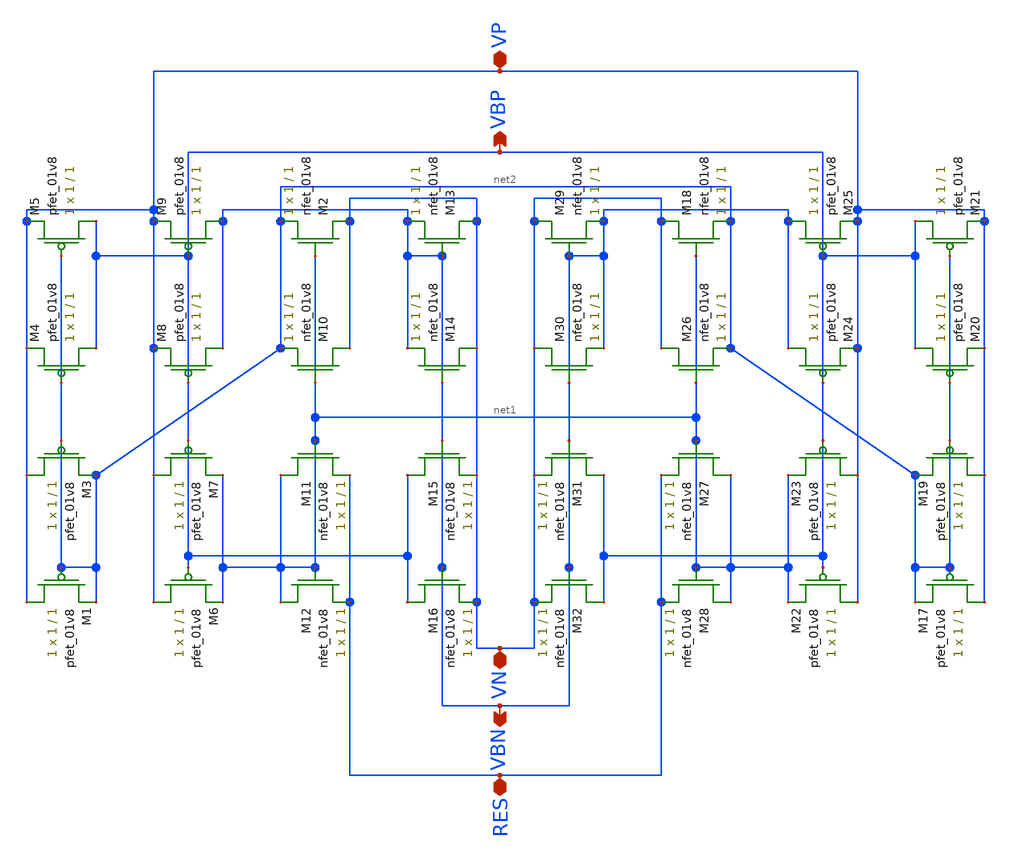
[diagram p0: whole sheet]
** sch_path: LDS/LDS_bbg.sch
**.subckt LDS_bbg VN VBN RES VP VBP
*.iopin VN
*.opin VBN
*.iopin RES
*.iopin VP
*.opin VBP
XM1 VP net2 net2 VDD sky130_fd_pr__pfet_01v8 L=1 W=1 nf=1 ad='int((nf+1)/2) * W/nf * 0.29' as='int((nf+2)/2) * W/nf * 0.29'
+ pd='2*int((nf+1)/2) * (W/nf + 0.29)' ps='2*int((nf+2)/2) * (W/nf + 0.29)' nrd='0.29 / W' nrs='0.29 / W'
+ sa=0 sb=0 sd=0 mult=1 m=1
XM2 VN net1 net2 GND sky130_fd_pr__nfet_01v8 L=1 W=1 nf=1 ad='int((nf+1)/2) * W/nf * 0.29' as='int((nf+2)/2) * W/nf * 0.29'
+ pd='2*int((nf+1)/2) * (W/nf + 0.29)' ps='2*int((nf+2)/2) * (W/nf + 0.29)' nrd='0.29 / W' nrs='0.29 / W'
+ sa=0 sb=0 sd=0 mult=1 m=1
XM3 VP net2 net2 VDD sky130_fd_pr__pfet_01v8 L=1 W=1 nf=1 ad='int((nf+1)/2) * W/nf * 0.29' as='int((nf+2)/2) * W/nf * 0.29'
+ pd='2*int((nf+1)/2) * (W/nf + 0.29)' ps='2*int((nf+2)/2) * (W/nf + 0.29)' nrd='0.29 / W' nrs='0.29 / W'
+ sa=0 sb=0 sd=0 mult=1 m=1
XM4 VBP net2 VP VDD sky130_fd_pr__pfet_01v8 L=1 W=1 nf=1 ad='int((nf+1)/2) * W/nf * 0.29' as='int((nf+2)/2) * W/nf * 0.29'
+ pd='2*int((nf+1)/2) * (W/nf + 0.29)' ps='2*int((nf+2)/2) * (W/nf + 0.29)' nrd='0.29 / W' nrs='0.29 / W'
+ sa=0 sb=0 sd=0 mult=1 m=1
XM5 VBP net2 VP VDD sky130_fd_pr__pfet_01v8 L=1 W=1 nf=1 ad='int((nf+1)/2) * W/nf * 0.29' as='int((nf+2)/2) * W/nf * 0.29'
+ pd='2*int((nf+1)/2) * (W/nf + 0.29)' ps='2*int((nf+2)/2) * (W/nf + 0.29)' nrd='0.29 / W' nrs='0.29 / W'
+ sa=0 sb=0 sd=0 mult=1 m=1
XM6 VP VBP net1 VDD sky130_fd_pr__pfet_01v8 L=1 W=1 nf=1 ad='int((nf+1)/2) * W/nf * 0.29' as='int((nf+2)/2) * W/nf * 0.29'
+ pd='2*int((nf+1)/2) * (W/nf + 0.29)' ps='2*int((nf+2)/2) * (W/nf + 0.29)' nrd='0.29 / W' nrs='0.29 / W'
+ sa=0 sb=0 sd=0 mult=1 m=1
XM7 VP VBP net1 VDD sky130_fd_pr__pfet_01v8 L=1 W=1 nf=1 ad='int((nf+1)/2) * W/nf * 0.29' as='int((nf+2)/2) * W/nf * 0.29'
+ pd='2*int((nf+1)/2) * (W/nf + 0.29)' ps='2*int((nf+2)/2) * (W/nf + 0.29)' nrd='0.29 / W' nrs='0.29 / W'
+ sa=0 sb=0 sd=0 mult=1 m=1
XM8 VBN VBP VP VDD sky130_fd_pr__pfet_01v8 L=1 W=1 nf=1 ad='int((nf+1)/2) * W/nf * 0.29' as='int((nf+2)/2) * W/nf * 0.29'
+ pd='2*int((nf+1)/2) * (W/nf + 0.29)' ps='2*int((nf+2)/2) * (W/nf + 0.29)' nrd='0.29 / W' nrs='0.29 / W'
+ sa=0 sb=0 sd=0 mult=1 m=1
XM9 VBN VBP VP VDD sky130_fd_pr__pfet_01v8 L=1 W=1 nf=1 ad='int((nf+1)/2) * W/nf * 0.29' as='int((nf+2)/2) * W/nf * 0.29'
+ pd='2*int((nf+1)/2) * (W/nf + 0.29)' ps='2*int((nf+2)/2) * (W/nf + 0.29)' nrd='0.29 / W' nrs='0.29 / W'
+ sa=0 sb=0 sd=0 mult=1 m=1
XM10 VN net1 net2 GND sky130_fd_pr__nfet_01v8 L=1 W=1 nf=1 ad='int((nf+1)/2) * W/nf * 0.29' as='int((nf+2)/2) * W/nf * 0.29'
+ pd='2*int((nf+1)/2) * (W/nf + 0.29)' ps='2*int((nf+2)/2) * (W/nf + 0.29)' nrd='0.29 / W' nrs='0.29 / W'
+ sa=0 sb=0 sd=0 mult=1 m=1
XM11 net1 net1 RES GND sky130_fd_pr__nfet_01v8 L=1 W=1 nf=1 ad='int((nf+1)/2) * W/nf * 0.29' as='int((nf+2)/2) * W/nf * 0.29'
+ pd='2*int((nf+1)/2) * (W/nf + 0.29)' ps='2*int((nf+2)/2) * (W/nf + 0.29)' nrd='0.29 / W' nrs='0.29 / W'
+ sa=0 sb=0 sd=0 mult=1 m=1
XM12 net1 net1 RES GND sky130_fd_pr__nfet_01v8 L=1 W=1 nf=1 ad='int((nf+1)/2) * W/nf * 0.29' as='int((nf+2)/2) * W/nf * 0.29'
+ pd='2*int((nf+1)/2) * (W/nf + 0.29)' ps='2*int((nf+2)/2) * (W/nf + 0.29)' nrd='0.29 / W' nrs='0.29 / W'
+ sa=0 sb=0 sd=0 mult=1 m=1
XM13 VN VBN VBN GND sky130_fd_pr__nfet_01v8 L=1 W=1 nf=1 ad='int((nf+1)/2) * W/nf * 0.29' as='int((nf+2)/2) * W/nf * 0.29'
+ pd='2*int((nf+1)/2) * (W/nf + 0.29)' ps='2*int((nf+2)/2) * (W/nf + 0.29)' nrd='0.29 / W' nrs='0.29 / W'
+ sa=0 sb=0 sd=0 mult=1 m=1
XM14 VN VBN VBN GND sky130_fd_pr__nfet_01v8 L=1 W=1 nf=1 ad='int((nf+1)/2) * W/nf * 0.29' as='int((nf+2)/2) * W/nf * 0.29'
+ pd='2*int((nf+1)/2) * (W/nf + 0.29)' ps='2*int((nf+2)/2) * (W/nf + 0.29)' nrd='0.29 / W' nrs='0.29 / W'
+ sa=0 sb=0 sd=0 mult=1 m=1
XM15 VBP VBN VN GND sky130_fd_pr__nfet_01v8 L=1 W=1 nf=1 ad='int((nf+1)/2) * W/nf * 0.29' as='int((nf+2)/2) * W/nf * 0.29'
+ pd='2*int((nf+1)/2) * (W/nf + 0.29)' ps='2*int((nf+2)/2) * (W/nf + 0.29)' nrd='0.29 / W' nrs='0.29 / W'
+ sa=0 sb=0 sd=0 mult=1 m=1
XM16 VBP VBN VN GND sky130_fd_pr__nfet_01v8 L=1 W=1 nf=1 ad='int((nf+1)/2) * W/nf * 0.29' as='int((nf+2)/2) * W/nf * 0.29'
+ pd='2*int((nf+1)/2) * (W/nf + 0.29)' ps='2*int((nf+2)/2) * (W/nf + 0.29)' nrd='0.29 / W' nrs='0.29 / W'
+ sa=0 sb=0 sd=0 mult=1 m=1
XM17 VP net2 net2 VDD sky130_fd_pr__pfet_01v8 L=1 W=1 nf=1 ad='int((nf+1)/2) * W/nf * 0.29' as='int((nf+2)/2) * W/nf * 0.29'
+ pd='2*int((nf+1)/2) * (W/nf + 0.29)' ps='2*int((nf+2)/2) * (W/nf + 0.29)' nrd='0.29 / W' nrs='0.29 / W'
+ sa=0 sb=0 sd=0 mult=1 m=1
XM18 VN net1 net2 GND sky130_fd_pr__nfet_01v8 L=1 W=1 nf=1 ad='int((nf+1)/2) * W/nf * 0.29' as='int((nf+2)/2) * W/nf * 0.29'
+ pd='2*int((nf+1)/2) * (W/nf + 0.29)' ps='2*int((nf+2)/2) * (W/nf + 0.29)' nrd='0.29 / W' nrs='0.29 / W'
+ sa=0 sb=0 sd=0 mult=1 m=1
XM19 VP net2 net2 VDD sky130_fd_pr__pfet_01v8 L=1 W=1 nf=1 ad='int((nf+1)/2) * W/nf * 0.29' as='int((nf+2)/2) * W/nf * 0.29'
+ pd='2*int((nf+1)/2) * (W/nf + 0.29)' ps='2*int((nf+2)/2) * (W/nf + 0.29)' nrd='0.29 / W' nrs='0.29 / W'
+ sa=0 sb=0 sd=0 mult=1 m=1
XM20 VBP net2 VP VDD sky130_fd_pr__pfet_01v8 L=1 W=1 nf=1 ad='int((nf+1)/2) * W/nf * 0.29' as='int((nf+2)/2) * W/nf * 0.29'
+ pd='2*int((nf+1)/2) * (W/nf + 0.29)' ps='2*int((nf+2)/2) * (W/nf + 0.29)' nrd='0.29 / W' nrs='0.29 / W'
+ sa=0 sb=0 sd=0 mult=1 m=1
XM21 VBP net2 VP VDD sky130_fd_pr__pfet_01v8 L=1 W=1 nf=1 ad='int((nf+1)/2) * W/nf * 0.29' as='int((nf+2)/2) * W/nf * 0.29'
+ pd='2*int((nf+1)/2) * (W/nf + 0.29)' ps='2*int((nf+2)/2) * (W/nf + 0.29)' nrd='0.29 / W' nrs='0.29 / W'
+ sa=0 sb=0 sd=0 mult=1 m=1
XM22 VP VBP net1 VDD sky130_fd_pr__pfet_01v8 L=1 W=1 nf=1 ad='int((nf+1)/2) * W/nf * 0.29' as='int((nf+2)/2) * W/nf * 0.29'
+ pd='2*int((nf+1)/2) * (W/nf + 0.29)' ps='2*int((nf+2)/2) * (W/nf + 0.29)' nrd='0.29 / W' nrs='0.29 / W'
+ sa=0 sb=0 sd=0 mult=1 m=1
XM23 VP VBP net1 VDD sky130_fd_pr__pfet_01v8 L=1 W=1 nf=1 ad='int((nf+1)/2) * W/nf * 0.29' as='int((nf+2)/2) * W/nf * 0.29'
+ pd='2*int((nf+1)/2) * (W/nf + 0.29)' ps='2*int((nf+2)/2) * (W/nf + 0.29)' nrd='0.29 / W' nrs='0.29 / W'
+ sa=0 sb=0 sd=0 mult=1 m=1
XM24 VBN VBP VP VDD sky130_fd_pr__pfet_01v8 L=1 W=1 nf=1 ad='int((nf+1)/2) * W/nf * 0.29' as='int((nf+2)/2) * W/nf * 0.29'
+ pd='2*int((nf+1)/2) * (W/nf + 0.29)' ps='2*int((nf+2)/2) * (W/nf + 0.29)' nrd='0.29 / W' nrs='0.29 / W'
+ sa=0 sb=0 sd=0 mult=1 m=1
XM25 VBN VBP VP VDD sky130_fd_pr__pfet_01v8 L=1 W=1 nf=1 ad='int((nf+1)/2) * W/nf * 0.29' as='int((nf+2)/2) * W/nf * 0.29'
+ pd='2*int((nf+1)/2) * (W/nf + 0.29)' ps='2*int((nf+2)/2) * (W/nf + 0.29)' nrd='0.29 / W' nrs='0.29 / W'
+ sa=0 sb=0 sd=0 mult=1 m=1
XM26 VN net1 net2 GND sky130_fd_pr__nfet_01v8 L=1 W=1 nf=1 ad='int((nf+1)/2) * W/nf * 0.29' as='int((nf+2)/2) * W/nf * 0.29'
+ pd='2*int((nf+1)/2) * (W/nf + 0.29)' ps='2*int((nf+2)/2) * (W/nf + 0.29)' nrd='0.29 / W' nrs='0.29 / W'
+ sa=0 sb=0 sd=0 mult=1 m=1
XM27 net1 net1 RES GND sky130_fd_pr__nfet_01v8 L=1 W=1 nf=1 ad='int((nf+1)/2) * W/nf * 0.29' as='int((nf+2)/2) * W/nf * 0.29'
+ pd='2*int((nf+1)/2) * (W/nf + 0.29)' ps='2*int((nf+2)/2) * (W/nf + 0.29)' nrd='0.29 / W' nrs='0.29 / W'
+ sa=0 sb=0 sd=0 mult=1 m=1
XM28 net1 net1 RES GND sky130_fd_pr__nfet_01v8 L=1 W=1 nf=1 ad='int((nf+1)/2) * W/nf * 0.29' as='int((nf+2)/2) * W/nf * 0.29'
+ pd='2*int((nf+1)/2) * (W/nf + 0.29)' ps='2*int((nf+2)/2) * (W/nf + 0.29)' nrd='0.29 / W' nrs='0.29 / W'
+ sa=0 sb=0 sd=0 mult=1 m=1
XM29 VN VBN VBN GND sky130_fd_pr__nfet_01v8 L=1 W=1 nf=1 ad='int((nf+1)/2) * W/nf * 0.29' as='int((nf+2)/2) * W/nf * 0.29'
+ pd='2*int((nf+1)/2) * (W/nf + 0.29)' ps='2*int((nf+2)/2) * (W/nf + 0.29)' nrd='0.29 / W' nrs='0.29 / W'
+ sa=0 sb=0 sd=0 mult=1 m=1
XM30 VN VBN VBN GND sky130_fd_pr__nfet_01v8 L=1 W=1 nf=1 ad='int((nf+1)/2) * W/nf * 0.29' as='int((nf+2)/2) * W/nf * 0.29'
+ pd='2*int((nf+1)/2) * (W/nf + 0.29)' ps='2*int((nf+2)/2) * (W/nf + 0.29)' nrd='0.29 / W' nrs='0.29 / W'
+ sa=0 sb=0 sd=0 mult=1 m=1
XM31 VBP VBN VN GND sky130_fd_pr__nfet_01v8 L=1 W=1 nf=1 ad='int((nf+1)/2) * W/nf * 0.29' as='int((nf+2)/2) * W/nf * 0.29'
+ pd='2*int((nf+1)/2) * (W/nf + 0.29)' ps='2*int((nf+2)/2) * (W/nf + 0.29)' nrd='0.29 / W' nrs='0.29 / W'
+ sa=0 sb=0 sd=0 mult=1 m=1
XM32 VBP VBN VN GND sky130_fd_pr__nfet_01v8 L=1 W=1 nf=1 ad='int((nf+1)/2) * W/nf * 0.29' as='int((nf+2)/2) * W/nf * 0.29'
+ pd='2*int((nf+1)/2) * (W/nf + 0.29)' ps='2*int((nf+2)/2) * (W/nf + 0.29)' nrd='0.29 / W' nrs='0.29 / W'
+ sa=0 sb=0 sd=0 mult=1 m=1
**.ends
.end
